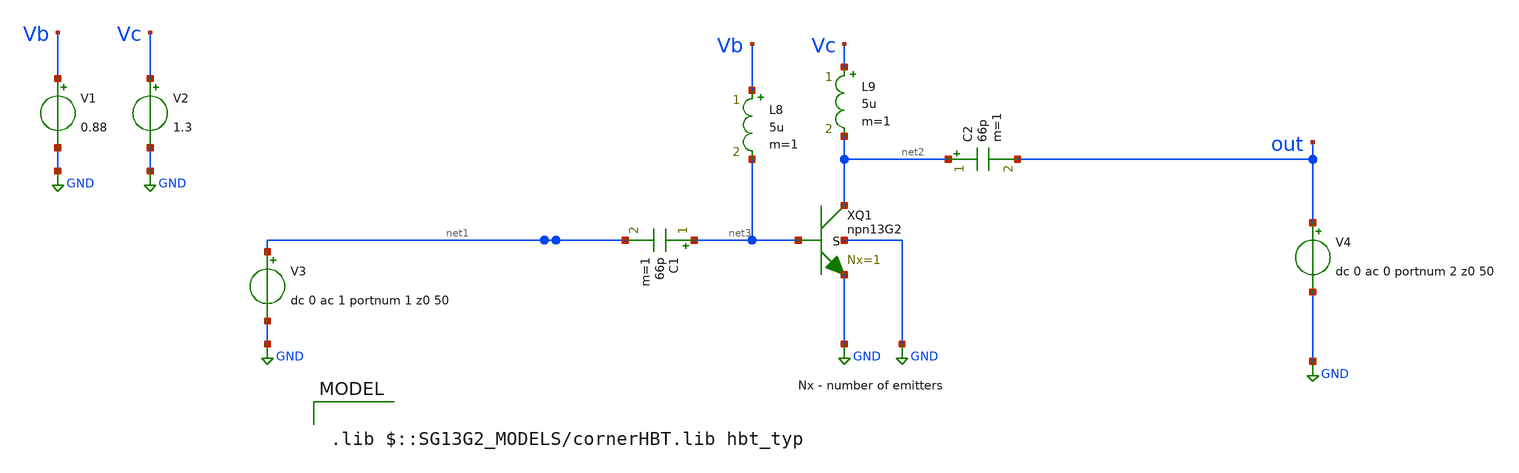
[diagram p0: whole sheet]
** sch_path: ihp-sg13g2/libs.tech/xschem/sg13g2_tests/sp_hbt_13g2_lna.sch
* Copyright 2023 IHP PDK Authors
**.subckt sp_hbt_13g2_lna
V4 out GND dc 0 ac 0 portnum 2 z0 50
XQ1 net2 net3 GND GND npn13G2 Nx=1
V3 net1 GND dc 0 ac 1 portnum 1 z0 50
V1 Vb GND 0.88
V2 Vc GND 1.3
C1 net3 net1 66p m=1
C2 net2 out 66p m=1
L8 Vb net3 5u m=1
L9 Vc net2 5u m=1
**** begin user architecture code

.lib $::SG13G2_MODELS/cornerHBT.lib hbt_typ



.param Rbase=50
.control
save all
sp dec 1000 9e7 1e11 1
let z11m = abs(z_1_1)
meas ac z11 FIND z11m AT=1e9
let phz=ph(z_1_1)
meas ac p11 FIND phz AT=1e9
let z22m = abs(z_2_2)
meas ac z22 FIND z22m AT=1e9
let phz22=ph(z_2_2)
meas ac p22 FIND phz22 AT=1e9


let s11m = abs(s_1_1)
meas ac s11 FIND s11m at=1e9
let phs11=ph(s_1_1)
meas ac ps11 FIND phs11 at=1e9

let s22m = abs(s_2_2)
meas ac s22 FIND s22m at=1e9
let phs22=ph(s_2_2)
meas ac ps22 FIND phs22 at=1e9

set color0 = white
set color1 = red
set color2 = blue
set xbrushwidth=5

*plot s_1_1 smithgrid
*plot z_1_1 smith

meas ac s21_max max s_2_1 from=9e8 to=5.1e9
write sp_hbt_13g2_lna.raw
*reset
*save all
*noise V(Vc) v3 lin 10k 9e8 1.1e9
*print inoise_total onoise_total
*setplot noise1
*write noise_hbt_13g2_lna.raw all
.endc


**** end user architecture code
**.ends
.GLOBAL GND
.end
